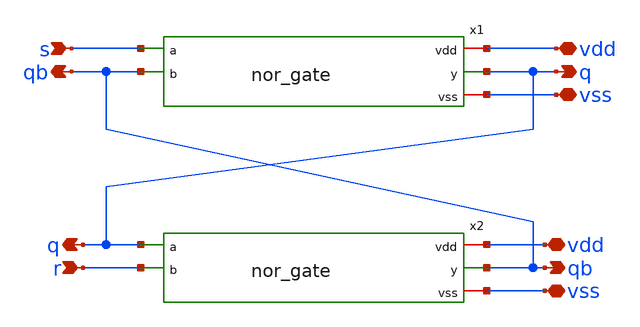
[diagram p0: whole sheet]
** sch_path: xschem/sr_latch.sch
**.subckt sr_latch s q r qb qb q vdd vss vdd vss
*.ipin s
*.opin q
*.ipin r
*.opin qb
*.opin qb
*.opin q
*.iopin vdd
*.iopin vss
*.iopin vdd
*.iopin vss
x1 vdd s q qb vss nor_gate
x2 vdd q qb r vss nor_gate
**.ends

* expanding   symbol:  nor_gate.sym # of pins=5
** sym_path: xschem/nor_gate.sym
** sch_path: xschem/nor_gate.sch
.subckt nor_gate vdd a y b vss
*.ipin a
*.ipin b
*.opin y
*.iopin vdd
*.iopin vss
XM1 net1 a vdd vdd sky130_fd_pr__pfet_01v8 L=0.15 W=1.5 nf=1 ad='int((nf+1)/2) * W/nf * 0.29' as='int((nf+2)/2) * W/nf * 0.29'
+ pd='2*int((nf+1)/2) * (W/nf + 0.29)' ps='2*int((nf+2)/2) * (W/nf + 0.29)' nrd='0.29 / W' nrs='0.29 / W'
+ sa=0 sb=0 sd=0 mult=1 m=1
XM2 y b net1 vdd sky130_fd_pr__pfet_01v8 L=0.15 W=1.5 nf=1 ad='int((nf+1)/2) * W/nf * 0.29' as='int((nf+2)/2) * W/nf * 0.29'
+ pd='2*int((nf+1)/2) * (W/nf + 0.29)' ps='2*int((nf+2)/2) * (W/nf + 0.29)' nrd='0.29 / W' nrs='0.29 / W'
+ sa=0 sb=0 sd=0 mult=1 m=1
XM3 y a vss vss sky130_fd_pr__nfet_01v8 L=0.15 W=0.75 nf=1 ad='int((nf+1)/2) * W/nf * 0.29' as='int((nf+2)/2) * W/nf * 0.29'
+ pd='2*int((nf+1)/2) * (W/nf + 0.29)' ps='2*int((nf+2)/2) * (W/nf + 0.29)' nrd='0.29 / W' nrs='0.29 / W'
+ sa=0 sb=0 sd=0 mult=1 m=1
XM4 y b vss vss sky130_fd_pr__nfet_01v8 L=0.15 W=0.75 nf=1 ad='int((nf+1)/2) * W/nf * 0.29' as='int((nf+2)/2) * W/nf * 0.29'
+ pd='2*int((nf+1)/2) * (W/nf + 0.29)' ps='2*int((nf+2)/2) * (W/nf + 0.29)' nrd='0.29 / W' nrs='0.29 / W'
+ sa=0 sb=0 sd=0 mult=1 m=1
.ends

.end
